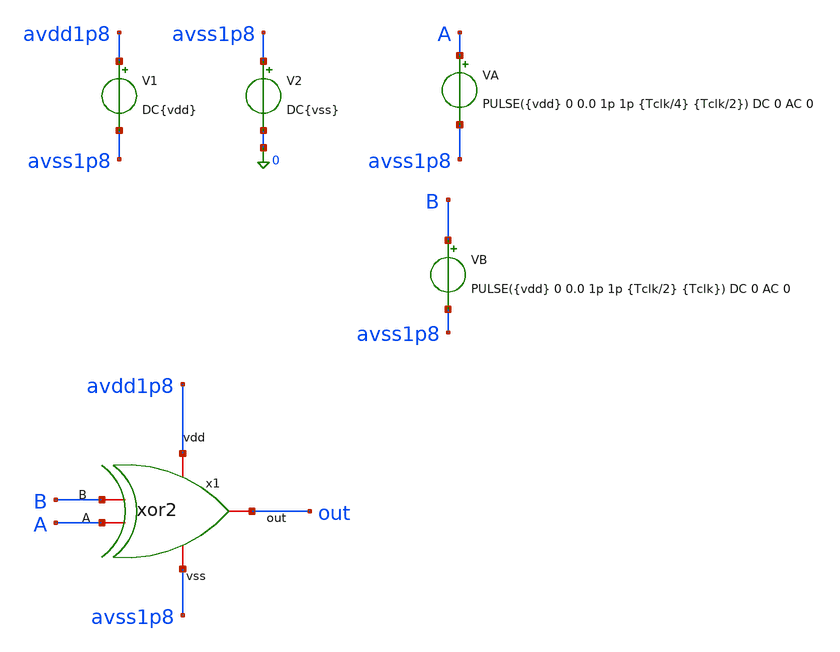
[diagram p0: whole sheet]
** sch_path: verification/testbenches/tb_xor2.sch
**.subckt tb_xor2
x1 avdd1p8 out B A avss1p8 xor2
V1 avdd1p8 avss1p8 DC{vdd}
V2 avss1p8 0 DC{vss}
VA A avss1p8 PULSE({vdd} 0 0.0 1p 1p {Tclk/4} {Tclk/2}) DC 0 AC 0
VB B avss1p8 PULSE({vdd} 0 0.0 1p 1p {Tclk/2} {Tclk}) DC 0 AC 0
**** begin user architecture code


* Circuit Parameters
.param vdd = 1.2
.param vss = 0.0
.param Tclk = 10n
.options TEMP = 27.0
* Include Models - IHP SG13G2
.lib cornerMOSlv.lib mos_tt
* OP Parameters & Singals to save
.save all
*Simulations
.control
tran 0.01u 100n
setplot tran1
plot v(A) v(B)+1.2 v(out)+3
reset
.endc
.end


**** end user architecture code
**.ends

* expanding   symbol:  blocks/xor2/schematic/xor2.sym # of pins=5
** sym_path: design/blocks/xor2/schematic/xor2.sym
** sch_path: design/blocks/xor2/schematic/xor2.sch
.subckt xor2 vdd out A B vss
*.iopin vdd
*.iopin vss
*.iopin out
*.iopin B
*.iopin A
XM4 out Ab net4 vss sg13_lv_nmos w=1.5u l=0.15u ng=1 m=1 mm_ok=1
XM6 net4 Bb vss vss sg13_lv_nmos w=1.5u l=0.15u ng=1 m=1 mm_ok=1
XM5 out A net3 vss sg13_lv_nmos w=1.5u l=0.15u ng=1 m=1 mm_ok=1
XM7 net3 B vss vss sg13_lv_nmos w=1.5u l=0.15u ng=1 m=1 mm_ok=1
XM9 Ab A vss vss sg13_lv_nmos w=0.75u l=0.15u ng=1 m=1 mm_ok=1
XM11 Bb B vss vss sg13_lv_nmos w=0.75u l=0.15u ng=1 m=1 mm_ok=1
XM2 out A net2 vdd sg13_lv_pmos w=1.5u l=0.15u ng=1 m=1 mm_ok=1
XM0 net2 Bb vdd vdd sg13_lv_pmos w=1.5u l=0.15u ng=1 m=1 mm_ok=1
XM3 out B net1 vdd sg13_lv_pmos w=1.5u l=0.15u ng=1 m=1 mm_ok=1
XM1 net1 Ab vdd vdd sg13_lv_pmos w=1.5u l=0.15u ng=1 m=1 mm_ok=1
XM8 Ab A vdd vdd sg13_lv_pmos w=1.5u l=0.15u ng=1 m=1 mm_ok=1
XM10 Bb B vdd vdd sg13_lv_pmos w=1.5u l=0.15u ng=1 m=1 mm_ok=1
.ends

.end
